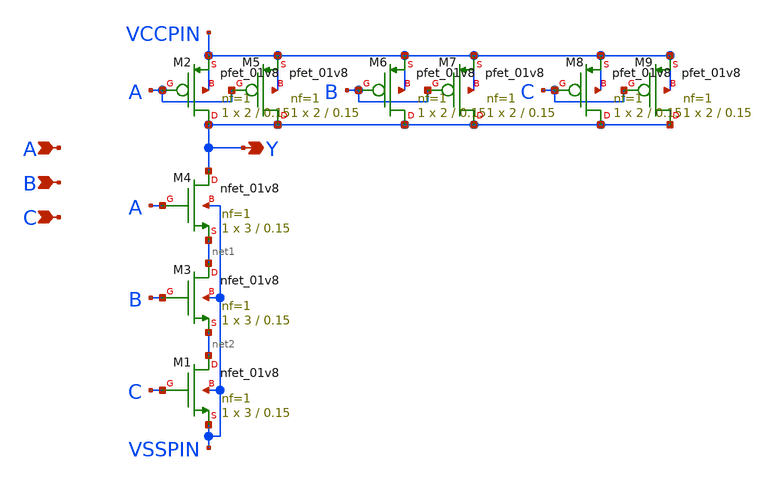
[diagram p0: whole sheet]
** sch_path: lib/xschem/NAND3X1.sch
**.subckt NAND3X1 A Y B C
*.ipin A
*.opin Y
*.ipin B
*.ipin C
XM1 net2 C VSSPIN VSSPIN sky130_fd_pr__nfet_01v8 L=0.15 W=3 nf=1 ad='int((nf+1)/2) * W/nf * 0.29' as='int((nf+2)/2) * W/nf * 0.29'
+ pd='2*int((nf+1)/2) * (W/nf + 0.29)' ps='2*int((nf+2)/2) * (W/nf + 0.29)' nrd='0.29 / W' nrs='0.29 / W'
+ sa=0 sb=0 sd=0 mult=1 m=1
XM2 Y A VCCPIN VCCPIN sky130_fd_pr__pfet_01v8 L=0.15 W=2 nf=1 ad='int((nf+1)/2) * W/nf * 0.29' as='int((nf+2)/2) * W/nf * 0.29'
+ pd='2*int((nf+1)/2) * (W/nf + 0.29)' ps='2*int((nf+2)/2) * (W/nf + 0.29)' nrd='0.29 / W' nrs='0.29 / W'
+ sa=0 sb=0 sd=0 mult=1 m=1
XM3 net1 B net2 VSSPIN sky130_fd_pr__nfet_01v8 L=0.15 W=3 nf=1 ad='int((nf+1)/2) * W/nf * 0.29' as='int((nf+2)/2) * W/nf * 0.29'
+ pd='2*int((nf+1)/2) * (W/nf + 0.29)' ps='2*int((nf+2)/2) * (W/nf + 0.29)' nrd='0.29 / W' nrs='0.29 / W'
+ sa=0 sb=0 sd=0 mult=1 m=1
XM4 Y A net1 VSSPIN sky130_fd_pr__nfet_01v8 L=0.15 W=3 nf=1 ad='int((nf+1)/2) * W/nf * 0.29' as='int((nf+2)/2) * W/nf * 0.29'
+ pd='2*int((nf+1)/2) * (W/nf + 0.29)' ps='2*int((nf+2)/2) * (W/nf + 0.29)' nrd='0.29 / W' nrs='0.29 / W'
+ sa=0 sb=0 sd=0 mult=1 m=1
XM5 Y A VCCPIN VCCPIN sky130_fd_pr__pfet_01v8 L=0.15 W=2 nf=1 ad='int((nf+1)/2) * W/nf * 0.29' as='int((nf+2)/2) * W/nf * 0.29'
+ pd='2*int((nf+1)/2) * (W/nf + 0.29)' ps='2*int((nf+2)/2) * (W/nf + 0.29)' nrd='0.29 / W' nrs='0.29 / W'
+ sa=0 sb=0 sd=0 mult=1 m=1
XM6 Y B VCCPIN VCCPIN sky130_fd_pr__pfet_01v8 L=0.15 W=2 nf=1 ad='int((nf+1)/2) * W/nf * 0.29' as='int((nf+2)/2) * W/nf * 0.29'
+ pd='2*int((nf+1)/2) * (W/nf + 0.29)' ps='2*int((nf+2)/2) * (W/nf + 0.29)' nrd='0.29 / W' nrs='0.29 / W'
+ sa=0 sb=0 sd=0 mult=1 m=1
XM7 Y B VCCPIN VCCPIN sky130_fd_pr__pfet_01v8 L=0.15 W=2 nf=1 ad='int((nf+1)/2) * W/nf * 0.29' as='int((nf+2)/2) * W/nf * 0.29'
+ pd='2*int((nf+1)/2) * (W/nf + 0.29)' ps='2*int((nf+2)/2) * (W/nf + 0.29)' nrd='0.29 / W' nrs='0.29 / W'
+ sa=0 sb=0 sd=0 mult=1 m=1
XM8 Y C VCCPIN VCCPIN sky130_fd_pr__pfet_01v8 L=0.15 W=2 nf=1 ad='int((nf+1)/2) * W/nf * 0.29' as='int((nf+2)/2) * W/nf * 0.29'
+ pd='2*int((nf+1)/2) * (W/nf + 0.29)' ps='2*int((nf+2)/2) * (W/nf + 0.29)' nrd='0.29 / W' nrs='0.29 / W'
+ sa=0 sb=0 sd=0 mult=1 m=1
XM9 Y C VCCPIN VCCPIN sky130_fd_pr__pfet_01v8 L=0.15 W=2 nf=1 ad='int((nf+1)/2) * W/nf * 0.29' as='int((nf+2)/2) * W/nf * 0.29'
+ pd='2*int((nf+1)/2) * (W/nf + 0.29)' ps='2*int((nf+2)/2) * (W/nf + 0.29)' nrd='0.29 / W' nrs='0.29 / W'
+ sa=0 sb=0 sd=0 mult=1 m=1
**.ends
.end
